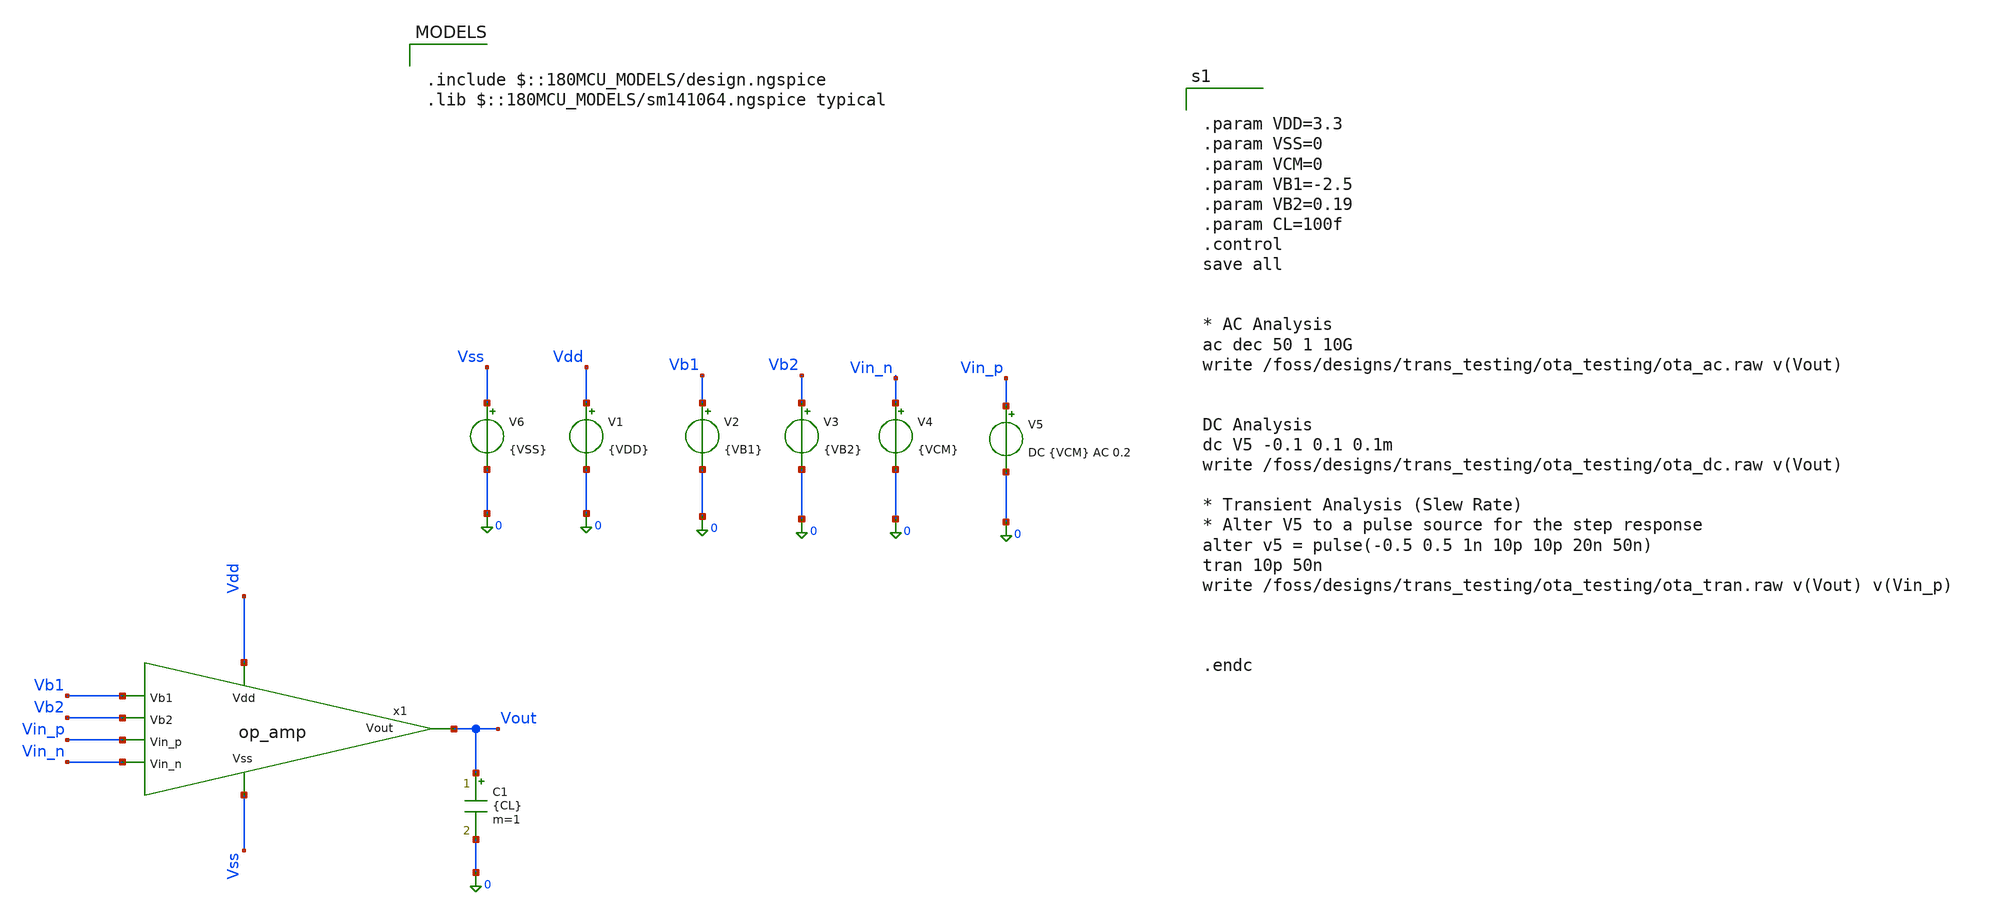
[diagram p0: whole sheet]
** sch_path: blocks/adc/lvds/ota_performance_test.sch
**.subckt ota_performance_test
x1 Vdd Vb1 Vout Vb2 Vin_p Vin_n Vss op_amp
V1 Vdd 0 {VDD}
V2 Vb1 0 {VB1}
V3 Vb2 0 {VB2}
V4 Vin_n 0 {VCM}
V5 Vin_p 0 DC {VCM} AC 0.2
V6 Vss 0 {VSS}
C1 Vout 0 {CL} m=1
**** begin user architecture code


.param VDD=3.3
.param VSS=0
.param VCM=0
.param VB1=-2.5
.param VB2=0.19
.param CL=100f
.control
save all


* AC Analysis
ac dec 50 1 10G
write /foss/designs/trans_testing/ota_testing/ota_ac.raw v(Vout)


DC Analysis
dc V5 -0.1 0.1 0.1m
write /foss/designs/trans_testing/ota_testing/ota_dc.raw v(Vout)

* Transient Analysis (Slew Rate)
* Alter V5 to a pulse source for the step response
alter v5 = pulse(-0.5 0.5 1n 10p 10p 20n 50n)
tran 10p 50n
write /foss/designs/trans_testing/ota_testing/ota_tran.raw v(Vout) v(Vin_p)



.endc



.include $::180MCU_MODELS/design.ngspice
.lib $::180MCU_MODELS/sm141064.ngspice typical

**** end user architecture code
**.ends

* expanding   symbol:  op_amp.sym # of pins=7
** sym_path: blocks/adc/lvds/op_amp.sym
** sch_path: blocks/adc/lvds/op_amp.sch
.subckt op_amp Vdd Vb1 Vout Vb2 Vin_p Vin_n Vss
*.ipin Vdd
*.ipin Vb2
*.ipin Vin_p
*.ipin Vin_n
*.ipin Vb1
*.opin Vout
*.ipin Vss
XM1 VdM1 vgM1 Vdd Vdd pfet_03v3 L=0.28u W=10.5u nf=1 ad='int((nf+1)/2) * W/nf * 0.18u' as='int((nf+2)/2) * W/nf * 0.18u'
+ pd='2*int((nf+1)/2) * (W/nf + 0.18u)' ps='2*int((nf+2)/2) * (W/nf + 0.18u)' nrd='0.18u / W' nrs='0.18u / W'
+ sa=0 sb=0 sd=0 m=1
XM2 VdM2 VdM4 Vdd Vdd pfet_03v3 L=0.28u W=10.5u nf=1 ad='int((nf+1)/2) * W/nf * 0.18u' as='int((nf+2)/2) * W/nf * 0.18u'
+ pd='2*int((nf+1)/2) * (W/nf + 0.18u)' ps='2*int((nf+2)/2) * (W/nf + 0.18u)' nrd='0.18u / W' nrs='0.18u / W'
+ sa=0 sb=0 sd=0 m=1
XM3 vgM1 Vb2 VdM1 Vdd pfet_03v3 L=0.28u W=10.5u nf=1 ad='int((nf+1)/2) * W/nf * 0.18u' as='int((nf+2)/2) * W/nf * 0.18u'
+ pd='2*int((nf+1)/2) * (W/nf + 0.18u)' ps='2*int((nf+2)/2) * (W/nf + 0.18u)' nrd='0.18u / W' nrs='0.18u / W'
+ sa=0 sb=0 sd=0 m=1
XM4 VdM4 Vb2 VdM2 Vdd pfet_03v3 L=0.28u W=10.5u nf=1 ad='int((nf+1)/2) * W/nf * 0.18u' as='int((nf+2)/2) * W/nf * 0.18u'
+ pd='2*int((nf+1)/2) * (W/nf + 0.18u)' ps='2*int((nf+2)/2) * (W/nf + 0.18u)' nrd='0.18u / W' nrs='0.18u / W'
+ sa=0 sb=0 sd=0 m=1
XM5 VdM4 Vin_p VsM5 Vdd nfet_03v3 L=0.28u W=52.5u nf=15 ad='int((nf+1)/2) * W/nf * 0.18u' as='int((nf+2)/2) * W/nf * 0.18u'
+ pd='2*int((nf+1)/2) * (W/nf + 0.18u)' ps='2*int((nf+2)/2) * (W/nf + 0.18u)' nrd='0.18u / W' nrs='0.18u / W'
+ sa=0 sb=0 sd=0 m=1
XM6 vgM1 Vin_n VsM5 Vdd nfet_03v3 L=0.28u W=52.5u nf=15 ad='int((nf+1)/2) * W/nf * 0.18u' as='int((nf+2)/2) * W/nf * 0.18u'
+ pd='2*int((nf+1)/2) * (W/nf + 0.18u)' ps='2*int((nf+2)/2) * (W/nf + 0.18u)' nrd='0.18u / W' nrs='0.18u / W'
+ sa=0 sb=0 sd=0 m=1
XM7 VdM7 VdM4 Vdd Vdd pfet_03v3 L=0.28u W=10.5u nf=1 ad='int((nf+1)/2) * W/nf * 0.18u' as='int((nf+2)/2) * W/nf * 0.18u'
+ pd='2*int((nf+1)/2) * (W/nf + 0.18u)' ps='2*int((nf+2)/2) * (W/nf + 0.18u)' nrd='0.18u / W' nrs='0.18u / W'
+ sa=0 sb=0 sd=0 m=1
XM9 VdM9 vgM1 Vdd Vdd pfet_03v3 L=0.28u W=10.5u nf=1 ad='int((nf+1)/2) * W/nf * 0.18u' as='int((nf+2)/2) * W/nf * 0.18u'
+ pd='2*int((nf+1)/2) * (W/nf + 0.18u)' ps='2*int((nf+2)/2) * (W/nf + 0.18u)' nrd='0.18u / W' nrs='0.18u / W'
+ sa=0 sb=0 sd=0 m=1
XM11 VgM14 Vb2 net2 0 nfet_03v3 L=0.28u W=5.25u nf=1 ad='int((nf+1)/2) * W/nf * 0.18u' as='int((nf+2)/2) * W/nf * 0.18u'
+ pd='2*int((nf+1)/2) * (W/nf + 0.18u)' ps='2*int((nf+2)/2) * (W/nf + 0.18u)' nrd='0.18u / W' nrs='0.18u / W'
+ sa=0 sb=0 sd=0 m=1
XM12 Vout Vb2 net1 0 nfet_03v3 L=0.28u W=5.25u nf=1 ad='int((nf+1)/2) * W/nf * 0.18u' as='int((nf+2)/2) * W/nf * 0.18u'
+ pd='2*int((nf+1)/2) * (W/nf + 0.18u)' ps='2*int((nf+2)/2) * (W/nf + 0.18u)' nrd='0.18u / W' nrs='0.18u / W'
+ sa=0 sb=0 sd=0 m=1
XM13 net2 VgM14 0 0 nfet_03v3 L=0.28u W=5.25u nf=1 ad='int((nf+1)/2) * W/nf * 0.18u' as='int((nf+2)/2) * W/nf * 0.18u'
+ pd='2*int((nf+1)/2) * (W/nf + 0.18u)' ps='2*int((nf+2)/2) * (W/nf + 0.18u)' nrd='0.18u / W' nrs='0.18u / W'
+ sa=0 sb=0 sd=0 m=1
XM14 net1 VgM14 0 0 nfet_03v3 L=0.28u W=5.25u nf=1 ad='int((nf+1)/2) * W/nf * 0.18u' as='int((nf+2)/2) * W/nf * 0.18u'
+ pd='2*int((nf+1)/2) * (W/nf + 0.18u)' ps='2*int((nf+2)/2) * (W/nf + 0.18u)' nrd='0.18u / W' nrs='0.18u / W'
+ sa=0 sb=0 sd=0 m=1
ibias VsM5 Vss 250u
XM8 VgM14 Vb1 VdM7 Vdd pfet_03v3 L=0.28u W=10.5u nf=1 ad='int((nf+1)/2) * W/nf * 0.18u' as='int((nf+2)/2) * W/nf * 0.18u'
+ pd='2*int((nf+1)/2) * (W/nf + 0.18u)' ps='2*int((nf+2)/2) * (W/nf + 0.18u)' nrd='0.18u / W' nrs='0.18u / W'
+ sa=0 sb=0 sd=0 m=1
XM10 Vout Vb1 VdM9 Vdd pfet_03v3 L=0.28u W=10.5u nf=1 ad='int((nf+1)/2) * W/nf * 0.18u' as='int((nf+2)/2) * W/nf * 0.18u'
+ pd='2*int((nf+1)/2) * (W/nf + 0.18u)' ps='2*int((nf+2)/2) * (W/nf + 0.18u)' nrd='0.18u / W' nrs='0.18u / W'
+ sa=0 sb=0 sd=0 m=1
.ends

.end
